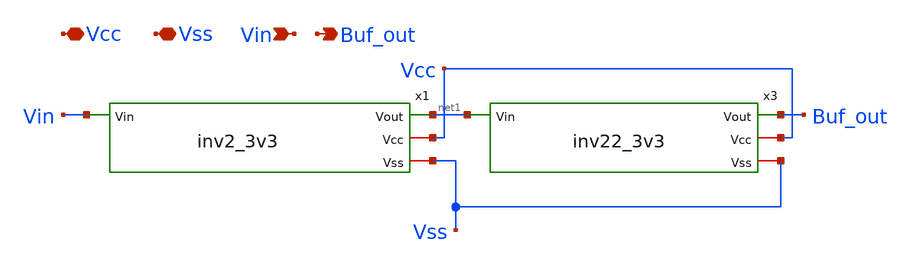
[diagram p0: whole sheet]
** sch_path: Git Files/Schematic/Pre Emphasis Driver/buf2_3v3.sch
**.subckt buf2_3v3 Vcc Vss Vin Buf_out
*.iopin Vcc
*.iopin Vss
*.ipin Vin
*.opin Buf_out
x1 Vin net1 Vcc Vss inv2_3v3
x3 net1 Buf_out Vcc Vss inv22_3v3
**.ends

* expanding   symbol:  /home/saumeek/simulation_library/inv2_3v3.sym # of pins=4
** sym_path: Git Files/Schematic/Pre Emphasis Driver/buf2_3v3/inv2_3v3.sym
** sch_path: Git Files/Schematic/Pre Emphasis Driver/buf2_3v3/inv2_3v3.sch
.subckt inv2_3v3 Vin Vout Vcc Vss
*.ipin Vin
*.opin Vout
*.iopin Vcc
*.iopin Vss
XM3 Vout Vin Vss Vss sky130_fd_pr__nfet_g5v0d10v5 L=0.5 W=15 nf=4 ad='int((nf+1)/2) * W/nf * 0.29' as='int((nf+2)/2) * W/nf * 0.29'
+ pd='2*int((nf+1)/2) * (W/nf + 0.29)' ps='2*int((nf+2)/2) * (W/nf + 0.29)' nrd='0.29 / W' nrs='0.29 / W'
+ sa=0 sb=0 sd=0 mult=1 m=1
XM1 Vout Vin Vcc Vcc sky130_fd_pr__pfet_g5v0d10v5 L=0.5 W=3 nf=1 ad='int((nf+1)/2) * W/nf * 0.29' as='int((nf+2)/2) * W/nf * 0.29'
+ pd='2*int((nf+1)/2) * (W/nf + 0.29)' ps='2*int((nf+2)/2) * (W/nf + 0.29)' nrd='0.29 / W' nrs='0.29 / W'
+ sa=0 sb=0 sd=0 mult=1 m=1
.ends


* expanding   symbol:  /home/saumeek/simulation_library/inv22_3v3.sym # of pins=4
** sym_path: Git Files/Schematic/Pre Emphasis Driver/buf2_3v3/inv22_3v3.sym
** sch_path: Git Files/Schematic/Pre Emphasis Driver/buf2_3v3/inv22_3v3.sch
.subckt inv22_3v3 Vin Vout Vcc Vss
*.ipin Vin
*.opin Vout
*.iopin Vcc
*.iopin Vss
XM3 Vout Vin Vcc Vcc sky130_fd_pr__pfet_g5v0d10v5 L=0.5 W=20 nf=5 ad='int((nf+1)/2) * W/nf * 0.29' as='int((nf+2)/2) * W/nf * 0.29'
+ pd='2*int((nf+1)/2) * (W/nf + 0.29)' ps='2*int((nf+2)/2) * (W/nf + 0.29)' nrd='0.29 / W' nrs='0.29 / W'
+ sa=0 sb=0 sd=0 mult=1 m=1
XM4 Vout Vin Vss Vss sky130_fd_pr__nfet_g5v0d10v5 L=0.5 W=5 nf=1 ad='int((nf+1)/2) * W/nf * 0.29' as='int((nf+2)/2) * W/nf * 0.29'
+ pd='2*int((nf+1)/2) * (W/nf + 0.29)' ps='2*int((nf+2)/2) * (W/nf + 0.29)' nrd='0.29 / W' nrs='0.29 / W'
+ sa=0 sb=0 sd=0 mult=1 m=1
.ends

.end
